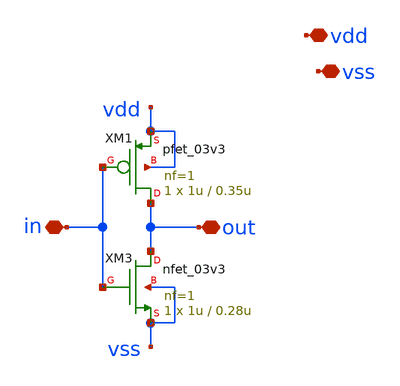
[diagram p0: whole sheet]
** sch_path: designs/libs/core_LIF_comp/core_not/not.sch
**.subckt not vdd vss in out
*.iopin vdd
*.iopin vss
*.iopin in
*.iopin out
XM1 out in vdd vdd pfet_03v3 L=0.35u W=1u nf=1 ad='int((nf+1)/2) * W/nf * 0.18u' as='int((nf+2)/2) * W/nf * 0.18u'
+ pd='2*int((nf+1)/2) * (W/nf + 0.18u)' ps='2*int((nf+2)/2) * (W/nf + 0.18u)' nrd='0.18u / W' nrs='0.18u / W'
+ sa=0 sb=0 sd=0 m=1
XM3 out in vss vss nfet_03v3 L=0.28u W=1u nf=1 ad='int((nf+1)/2) * W/nf * 0.18u' as='int((nf+2)/2) * W/nf * 0.18u'
+ pd='2*int((nf+1)/2) * (W/nf + 0.18u)' ps='2*int((nf+2)/2) * (W/nf + 0.18u)' nrd='0.18u / W' nrs='0.18u / W'
+ sa=0 sb=0 sd=0 m=1
**.ends
.end
